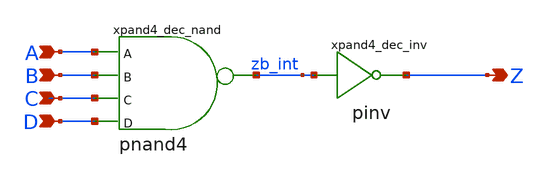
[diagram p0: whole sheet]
** sch_path: sram_4_16_scn4m/and4_dec.sch
**.subckt and4_dec A B C D Z
*.ipin A
*.ipin B
*.ipin C
*.ipin D
*.opin Z
xpand4_dec_nand A B C D zb_int vdd gnd pnand4
xpand4_dec_inv zb_int Z vdd gnd pinv
**.ends

* expanding   symbol:  pnand4.sym # of pins=5
** sym_path: sram_2_16_scn4m/pnand4.sym
** sch_path: sram_2_16_scn4m/pnand4.sch
.subckt pnand4 A B C D Z vdd gnd
*.ipin D
*.ipin C
*.ipin A
*.ipin B
*.opin Z
*.iopin vdd
*.iopin gnd
Mpnand4_nmos1 Z D net1 gnd n w=1.6u l=0.4u m=1
Mpnand3_pmos1 Z A vdd vdd p w=1.6u l=0.4u m=1
Mpnand4_pmos4 Z D vdd vdd p w=1.6u l=0.4u m=1
Mpnand4_nmos2 net1 C net2 gnd n w=1.6u l=0.4u m=1
Mpnand4_pmos3 Z C vdd vdd p w=1.6u l=0.4u m=1
Mpnand4_nmos3 net2 B net3 gnd n w=1.6u l=0.4u m=1
Mpnand4_pmos2 Z B vdd vdd p w=1.6u l=0.4u m=1
Mpnand4_nmos4 net3 A gnd gnd n w=1.6u l=0.4u m=1
.ends


* expanding   symbol:  pinv.sym # of pins=2
** sym_path: sram_4_16_scn4m/pinv.sym
** sch_path: sram_4_16_scn4m/pinv.sch
.subckt pinv A Z vdd gnd
*.ipin A
*.opin Z
Mpinv_nmos Z A gnd gnd n w=0.8u l=0.4u m=1
Mp_inv_pmos Z A vdd vdd p w=1.6u l=0.4u m=1
.ends

.end
